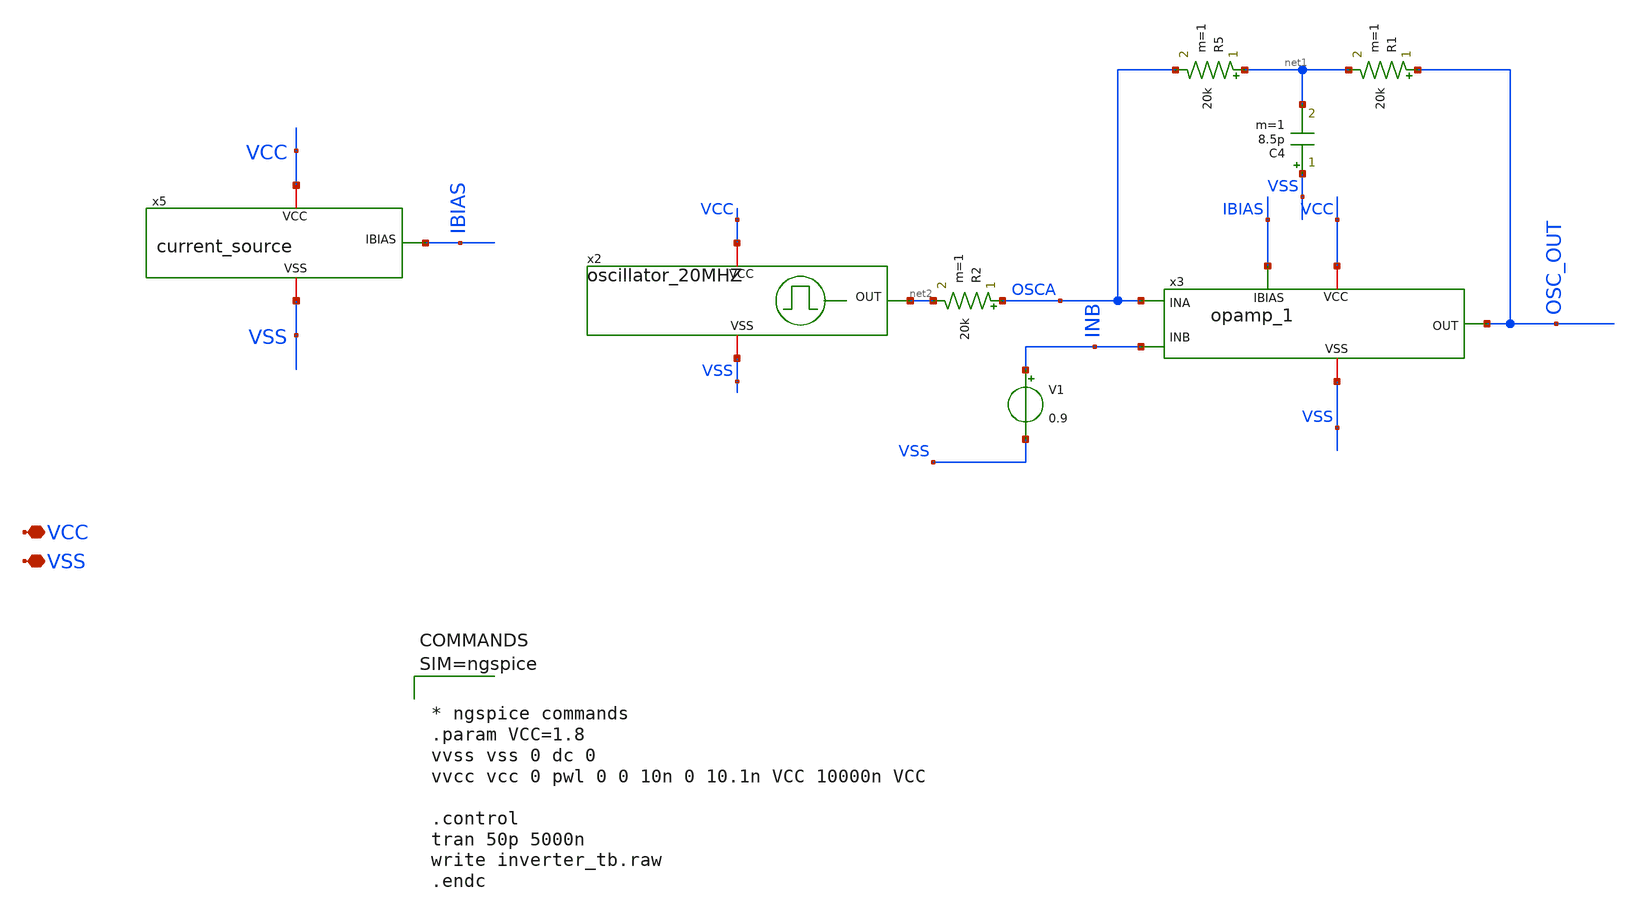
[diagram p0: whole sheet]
** sch_path: xschem/filter_oscillator_20mhz.sch
**.subckt filter_oscillator_20mhz VCC VSS
*.iopin VCC
*.iopin VSS
x5 VCC VSS IBIAS current_source
x2 VCC net2 VSS oscillator_20MHZ
x3 VCC OSC_OUT OSCA INB VSS IBIAS opamp_1
C4 VSS net1 8.5p m=1
R5 net1 OSCA 20k m=1
R1 OSC_OUT net1 20k m=1
V1 INB VSS 0.9
R2 OSCA net2 20k m=1
**** begin user architecture code

** opencircuitdesign pdks install
.lib $::SKYWATER_MODELS/sky130.lib.spice tt





* ngspice commands
.param VCC=1.8
vvss vss 0 dc 0
vvcc vcc 0 pwl 0 0 10n 0 10.1n VCC 10000n VCC

.control
tran 50p 5000n
write inverter_tb.raw
.endc




**** end user architecture code
**.ends

* expanding   symbol:  current_source.sym # of pins=3
** sym_path: xschem/current_source.sym
** sch_path: xschem/current_source.sch
.subckt current_source VCC VSS IBIAS
*.iopin VCC
*.iopin VSS
*.opin IBIAS
XM3 IBIAS IBIAS VSS VSS sky130_fd_pr__nfet_01v8 L=1 W=40 nf=1 ad='int((nf+1)/2) * W/nf * 0.29' as='int((nf+2)/2) * W/nf * 0.29'
+ pd='2*int((nf+1)/2) * (W/nf + 0.29)' ps='2*int((nf+2)/2) * (W/nf + 0.29)' nrd='0.29 / W' nrs='0.29 / W'
+ sa=0 sb=0 sd=0 mult=1 m=1
XR1 IBIAS VCC sky130_fd_pr__res_generic_po W=0.33 L=12 m=1
.ends


* expanding   symbol:  oscillator_20MHZ.sym # of pins=3
** sym_path: xschem/oscillator_20MHZ.sym
** sch_path: xschem/oscillator_20MHZ.sch
.subckt oscillator_20MHZ VCC OUT VSS
*.iopin VCC
*.iopin VSS
*.opin OUT
x1[20] INI[19] OUT_INI VCC VSS inverter
x1[19] INI[18] INI[19] VCC VSS inverter
x1[18] INI[17] INI[18] VCC VSS inverter
x1[17] INI[16] INI[17] VCC VSS inverter
x1[16] INI[15] INI[16] VCC VSS inverter
x1[15] INI[14] INI[15] VCC VSS inverter
x1[14] INI[13] INI[14] VCC VSS inverter
x1[13] INI[12] INI[13] VCC VSS inverter
x1[12] INI[11] INI[12] VCC VSS inverter
x1[11] INI[10] INI[11] VCC VSS inverter
x1[10] INI[9] INI[10] VCC VSS inverter
x1[9] INI[8] INI[9] VCC VSS inverter
x1[8] INI[7] INI[8] VCC VSS inverter
x1[7] INI[6] INI[7] VCC VSS inverter
x1[6] INI[5] INI[6] VCC VSS inverter
x1[5] INI[4] INI[5] VCC VSS inverter
x1[4] INI[3] INI[4] VCC VSS inverter
x1[3] INI[2] INI[3] VCC VSS inverter
x1[2] INI[1] INI[2] VCC VSS inverter
x1[1] INI[0] INI[1] VCC VSS inverter
x1[0] OUT_INI INI[0] VCC VSS inverter
x3 OUT OUT_INI VCC VSS inverter
.ends


* expanding   symbol:  opamp_1.sym # of pins=6
** sym_path: xschem/opamp_1.sym
** sch_path: xschem/opamp_1.sch
.subckt opamp_1 VCC OUT INA INB VSS IBIAS
*.ipin INA
*.ipin INB
*.opin OUT
*.iopin VCC
*.iopin VSS
*.ipin IBIAS
XM1 MIRR INA TAILV VSS sky130_fd_pr__nfet_01v8 L=1 W=20 nf=1 ad='int((nf+1)/2) * W/nf * 0.29' as='int((nf+2)/2) * W/nf * 0.29'
+ pd='2*int((nf+1)/2) * (W/nf + 0.29)' ps='2*int((nf+2)/2) * (W/nf + 0.29)' nrd='0.29 / W' nrs='0.29 / W'
+ sa=0 sb=0 sd=0 mult=1 m=1
XM2 DIFF_OUT INB TAILV VSS sky130_fd_pr__nfet_01v8 L=1 W=20 nf=1 ad='int((nf+1)/2) * W/nf * 0.29' as='int((nf+2)/2) * W/nf * 0.29'
+ pd='2*int((nf+1)/2) * (W/nf + 0.29)' ps='2*int((nf+2)/2) * (W/nf + 0.29)' nrd='0.29 / W' nrs='0.29 / W'
+ sa=0 sb=0 sd=0 mult=1 m=1
XM3 TAILV IBIAS VSS VSS sky130_fd_pr__nfet_01v8 L=1 W=40 nf=1 ad='int((nf+1)/2) * W/nf * 0.29' as='int((nf+2)/2) * W/nf * 0.29'
+ pd='2*int((nf+1)/2) * (W/nf + 0.29)' ps='2*int((nf+2)/2) * (W/nf + 0.29)' nrd='0.29 / W' nrs='0.29 / W'
+ sa=0 sb=0 sd=0 mult=1 m=1
XM4 MIRR MIRR VCC VCC sky130_fd_pr__pfet_01v8_lvt L=0.5 W=14 nf=1 ad='int((nf+1)/2) * W/nf * 0.29' as='int((nf+2)/2) * W/nf * 0.29'
+ pd='2*int((nf+1)/2) * (W/nf + 0.29)' ps='2*int((nf+2)/2) * (W/nf + 0.29)' nrd='0.29 / W' nrs='0.29 / W'
+ sa=0 sb=0 sd=0 mult=1 m=1
XM5 DIFF_OUT MIRR VCC VCC sky130_fd_pr__pfet_01v8_lvt L=0.5 W=14 nf=1 ad='int((nf+1)/2) * W/nf * 0.29'
+ as='int((nf+2)/2) * W/nf * 0.29' pd='2*int((nf+1)/2) * (W/nf + 0.29)' ps='2*int((nf+2)/2) * (W/nf + 0.29)'
+ nrd='0.29 / W' nrs='0.29 / W' sa=0 sb=0 sd=0 mult=1 m=1
XM6 OUT IBIAS VSS VSS sky130_fd_pr__nfet_01v8 L=0.5 W=93 nf=1 ad='int((nf+1)/2) * W/nf * 0.29' as='int((nf+2)/2) * W/nf * 0.29'
+ pd='2*int((nf+1)/2) * (W/nf + 0.29)' ps='2*int((nf+2)/2) * (W/nf + 0.29)' nrd='0.29 / W' nrs='0.29 / W'
+ sa=0 sb=0 sd=0 mult=1 m=1
XM7 OUT DIFF_OUT VCC VCC sky130_fd_pr__pfet_01v8_lvt L=0.5 W=70 nf=1 ad='int((nf+1)/2) * W/nf * 0.29'
+ as='int((nf+2)/2) * W/nf * 0.29' pd='2*int((nf+1)/2) * (W/nf + 0.29)' ps='2*int((nf+2)/2) * (W/nf + 0.29)'
+ nrd='0.29 / W' nrs='0.29 / W' sa=0 sb=0 sd=0 mult=1 m=1
XM9 RBIAS IBIAS VSS VSS sky130_fd_pr__nfet_01v8 L=1 W=5 nf=1 ad='int((nf+1)/2) * W/nf * 0.29' as='int((nf+2)/2) * W/nf * 0.29'
+ pd='2*int((nf+1)/2) * (W/nf + 0.29)' ps='2*int((nf+2)/2) * (W/nf + 0.29)' nrd='0.29 / W' nrs='0.29 / W'
+ sa=0 sb=0 sd=0 mult=1 m=1
XM10 RBIAS RBIAS net2 VCC sky130_fd_pr__pfet_01v8_lvt L=0.5 W=1 nf=1 ad='int((nf+1)/2) * W/nf * 0.29'
+ as='int((nf+2)/2) * W/nf * 0.29' pd='2*int((nf+1)/2) * (W/nf + 0.29)' ps='2*int((nf+2)/2) * (W/nf + 0.29)'
+ nrd='0.29 / W' nrs='0.29 / W' sa=0 sb=0 sd=0 mult=1 m=1
XM11 net2 net2 VCC VCC sky130_fd_pr__pfet_01v8_lvt L=0.5 W=7.5 nf=1 ad='int((nf+1)/2) * W/nf * 0.29'
+ as='int((nf+2)/2) * W/nf * 0.29' pd='2*int((nf+1)/2) * (W/nf + 0.29)' ps='2*int((nf+2)/2) * (W/nf + 0.29)'
+ nrd='0.29 / W' nrs='0.29 / W' sa=0 sb=0 sd=0 mult=1 m=1
XC1 OUT net1 sky130_fd_pr__cap_mim_m3_2 W=20 L=13 MF=1 m=1
XM8 net1 RBIAS DIFF_OUT VCC sky130_fd_pr__pfet_01v8_lvt L=0.5 W=14 nf=1 ad='int((nf+1)/2) * W/nf * 0.29'
+ as='int((nf+2)/2) * W/nf * 0.29' pd='2*int((nf+1)/2) * (W/nf + 0.29)' ps='2*int((nf+2)/2) * (W/nf + 0.29)'
+ nrd='0.29 / W' nrs='0.29 / W' sa=0 sb=0 sd=0 mult=1 m=1
.ends


* expanding   symbol:  inverter.sym # of pins=4
** sym_path: xschem/inverter.sym
** sch_path: xschem/inverter.sch
.subckt inverter OUT IN VCC VSS
*.iopin VCC
*.iopin VSS
*.ipin IN
*.opin OUT
XM1 OUT IN net1 VCC sky130_fd_pr__pfet_01v8 L=1 W=2 nf=1 ad='int((nf+1)/2) * W/nf * 0.29' as='int((nf+2)/2) * W/nf * 0.29'
+ pd='2*int((nf+1)/2) * (W/nf + 0.29)' ps='2*int((nf+2)/2) * (W/nf + 0.29)' nrd='0.29 / W' nrs='0.29 / W'
+ sa=0 sb=0 sd=0 mult=1 m=1
XM2 OUT IN net2 VSS sky130_fd_pr__nfet_01v8 L=1 W=1 nf=1 ad='int((nf+1)/2) * W/nf * 0.29' as='int((nf+2)/2) * W/nf * 0.29'
+ pd='2*int((nf+1)/2) * (W/nf + 0.29)' ps='2*int((nf+2)/2) * (W/nf + 0.29)' nrd='0.29 / W' nrs='0.29 / W'
+ sa=0 sb=0 sd=0 mult=1 m=1
XM3 net1 VSS VCC VCC sky130_fd_pr__pfet_01v8 L=1 W=2 nf=1 ad='int((nf+1)/2) * W/nf * 0.29' as='int((nf+2)/2) * W/nf * 0.29'
+ pd='2*int((nf+1)/2) * (W/nf + 0.29)' ps='2*int((nf+2)/2) * (W/nf + 0.29)' nrd='0.29 / W' nrs='0.29 / W'
+ sa=0 sb=0 sd=0 mult=1 m=1
XM4 net2 VCC VSS VSS sky130_fd_pr__nfet_01v8 L=1 W=1 nf=1 ad='int((nf+1)/2) * W/nf * 0.29' as='int((nf+2)/2) * W/nf * 0.29'
+ pd='2*int((nf+1)/2) * (W/nf + 0.29)' ps='2*int((nf+2)/2) * (W/nf + 0.29)' nrd='0.29 / W' nrs='0.29 / W'
+ sa=0 sb=0 sd=0 mult=1 m=1
.ends

.end
